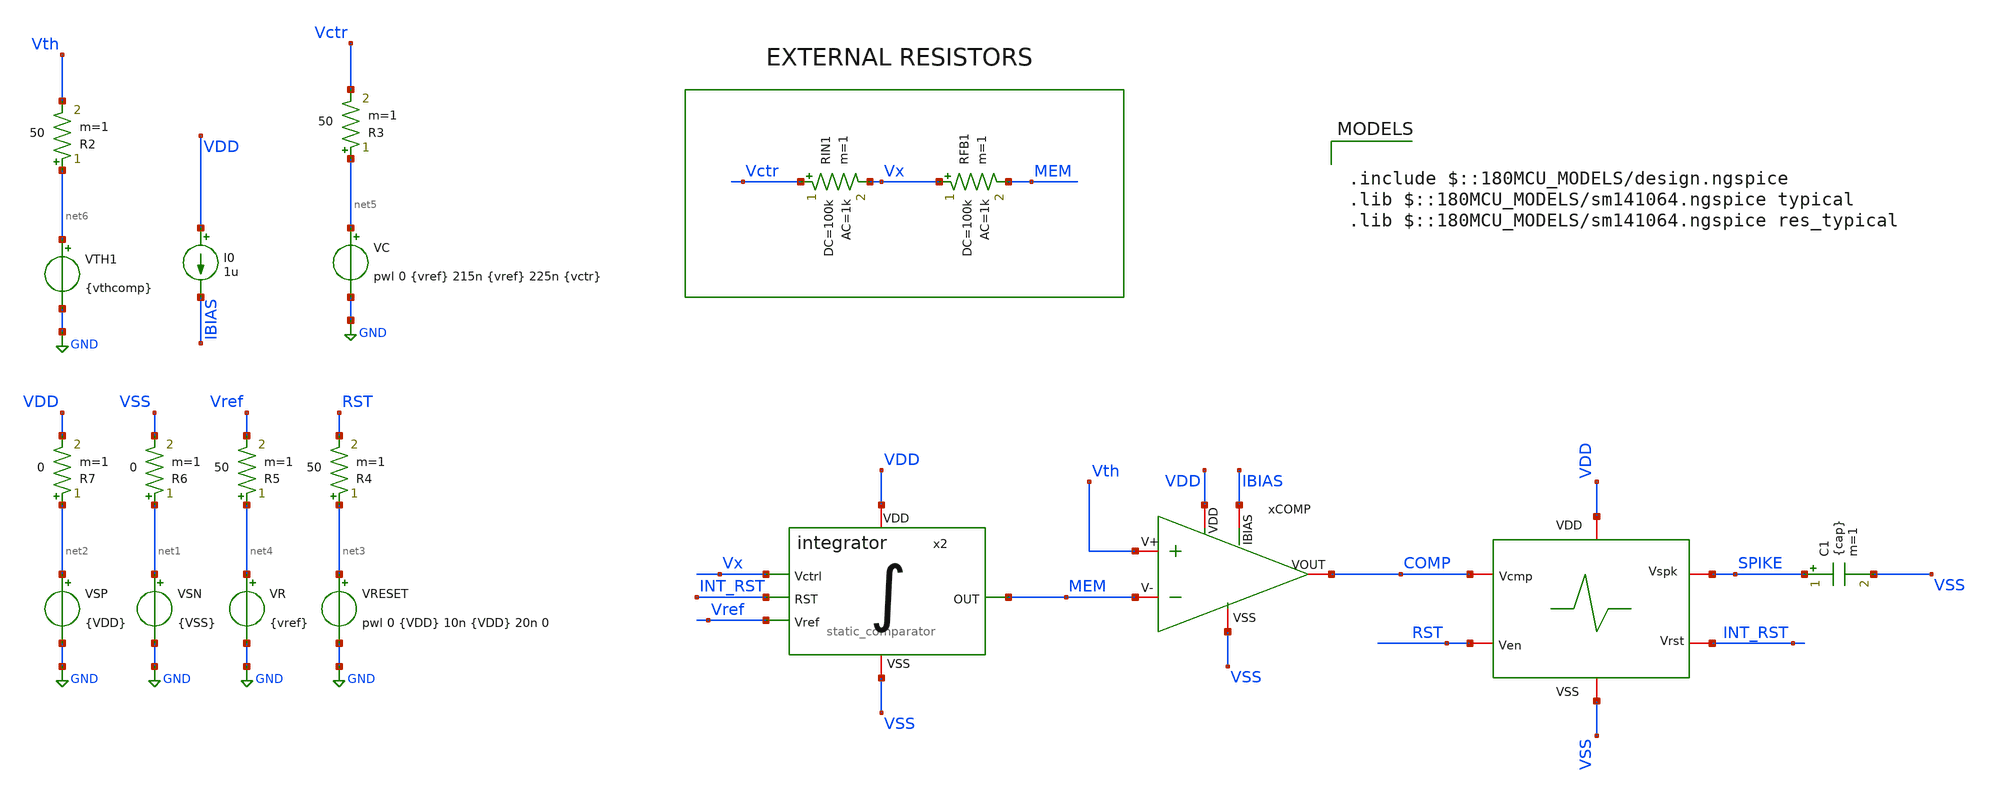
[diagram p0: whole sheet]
** sch_path: designs/LIF_Neuron/LIF_Neuron_TB.sch
**.subckt LIF_Neuron_TB
VRESET net3 GND pwl 0 {VDD} 10n {VDD} 20n 0
VSP net2 GND {VDD}
VSN net1 GND {VSS}
VR net4 GND {vref}
VC net5 GND pwl 0 {vref} 215n {vref} 225n {vctr}
xCOMP VDD IBIAS VSS Vth MEM COMP static_comparator
VTH1 net6 GND {vthcomp}
I0 VDD IBIAS 1u
R3 net5 Vctr 50 m=1
R2 net6 Vth 50 m=1
R4 net3 RST 50 m=1
R5 net4 Vref 50 m=1
R6 net1 VSS 0 m=1
R7 net2 VDD 0 m=1
x1 VDD COMP SPIKE INT_RST RST VSS spike_generator
x2 VDD Vx MEM INT_RST Vref VSS integrator
RIN1 Vctr Vx 100k ac=1k m=1
RFB1 Vx MEM 100k ac=1k m=1
C1 SPIKE VSS {cap} m=1
**** begin user architecture code

.include $::180MCU_MODELS/design.ngspice
.lib $::180MCU_MODELS/sm141064.ngspice typical
.lib $::180MCU_MODELS/sm141064.ngspice res_typical





.param VDD = 1.8
.param VSS = 0
.param vctr = 1.8
.param vref = 1.44
.param vthcomp = 1.2
.param cap = 15f

.param wxor=5.6u

.save all

.control

*----------------------------- Parámetros generales
let Vhigh = 1.8
let Vmid = Vhigh * 0.5

tran 0.1n 1u
meas tran IDD_AVG AVG i(VSP) from=20n to=1u
let PAVG = abs(IDD_AVG*Vhigh)
print PAVG

meas TRAN T_spk TRIG v(SPIKE) VAL=Vmid rise=2 TARG v(SPIKE) VAL=Vmid rise=3
let F_spk = 1 / T_spk
print F_spk

plot v(Vctr) v(Vref)
plot v(MEM) v(Vx)
plot v(COMP)
plot v(RST) v(INT_RST)
plot v(SPIKE)

.endc


**** end user architecture code
**.ends
.GLOBAL GND
.end
